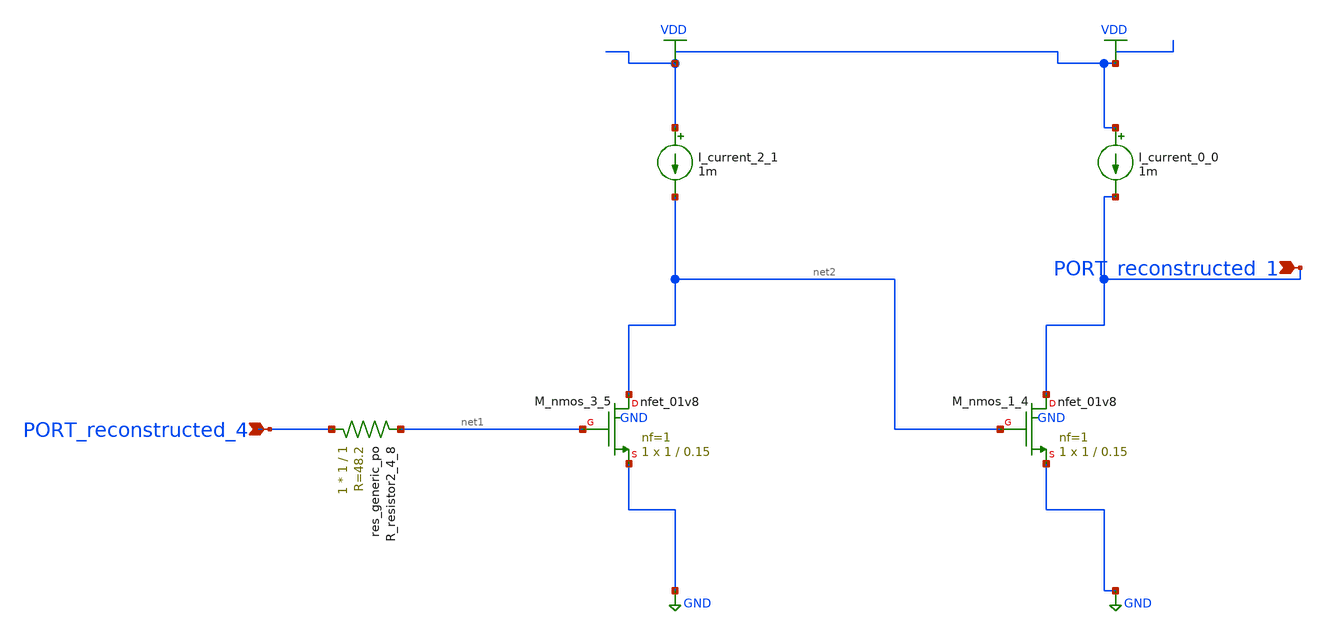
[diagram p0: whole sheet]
** sch_path: schematics/AMSNet/409.sch
**.subckt 409 PORT_reconstructed_1 PORT_reconstructed_4
*.ipin PORT_reconstructed_1
*.ipin PORT_reconstructed_4
I_current_0_0 VDD PORT_reconstructed_1 1m
I_current_2_1 VDD net2 1m
XM_nmos_1_4 PORT_reconstructed_1 net2 GND GND sky130_fd_pr__nfet_01v8 L=0.15 W=1 nf=1 ad='int((1 + 1)/2) * 1 / 1 * 0.29'
+ as='int((1 + 2)/2) * 1 / 1 * 0.29' pd='2*int((1 + 1)/2) * (1 / 1 + 0.29)' ps='2*int((1 + 2)/2) * (1 / 1 + 0.29)'
+ nrd='0.29 / 1 ' nrs='0.29 / 1 ' sa=0 sb=0 sd=0 mult=1 m=1
XM_nmos_3_5 net2 net1 GND GND sky130_fd_pr__nfet_01v8 L=0.15 W=1 nf=1 ad='int((1 + 1)/2) * 1 / 1 * 0.29'
+ as='int((1 + 2)/2) * 1 / 1 * 0.29' pd='2*int((1 + 1)/2) * (1 / 1 + 0.29)' ps='2*int((1 + 2)/2) * (1 / 1 + 0.29)'
+ nrd='0.29 / 1 ' nrs='0.29 / 1 ' sa=0 sb=0 sd=0 mult=1 m=1
XR_resistor2_4_8 PORT_reconstructed_4 net1 sky130_fd_pr__res_generic_po W=1 L=1 m=1
**.ends
.GLOBAL GND
.GLOBAL VDD
.end
